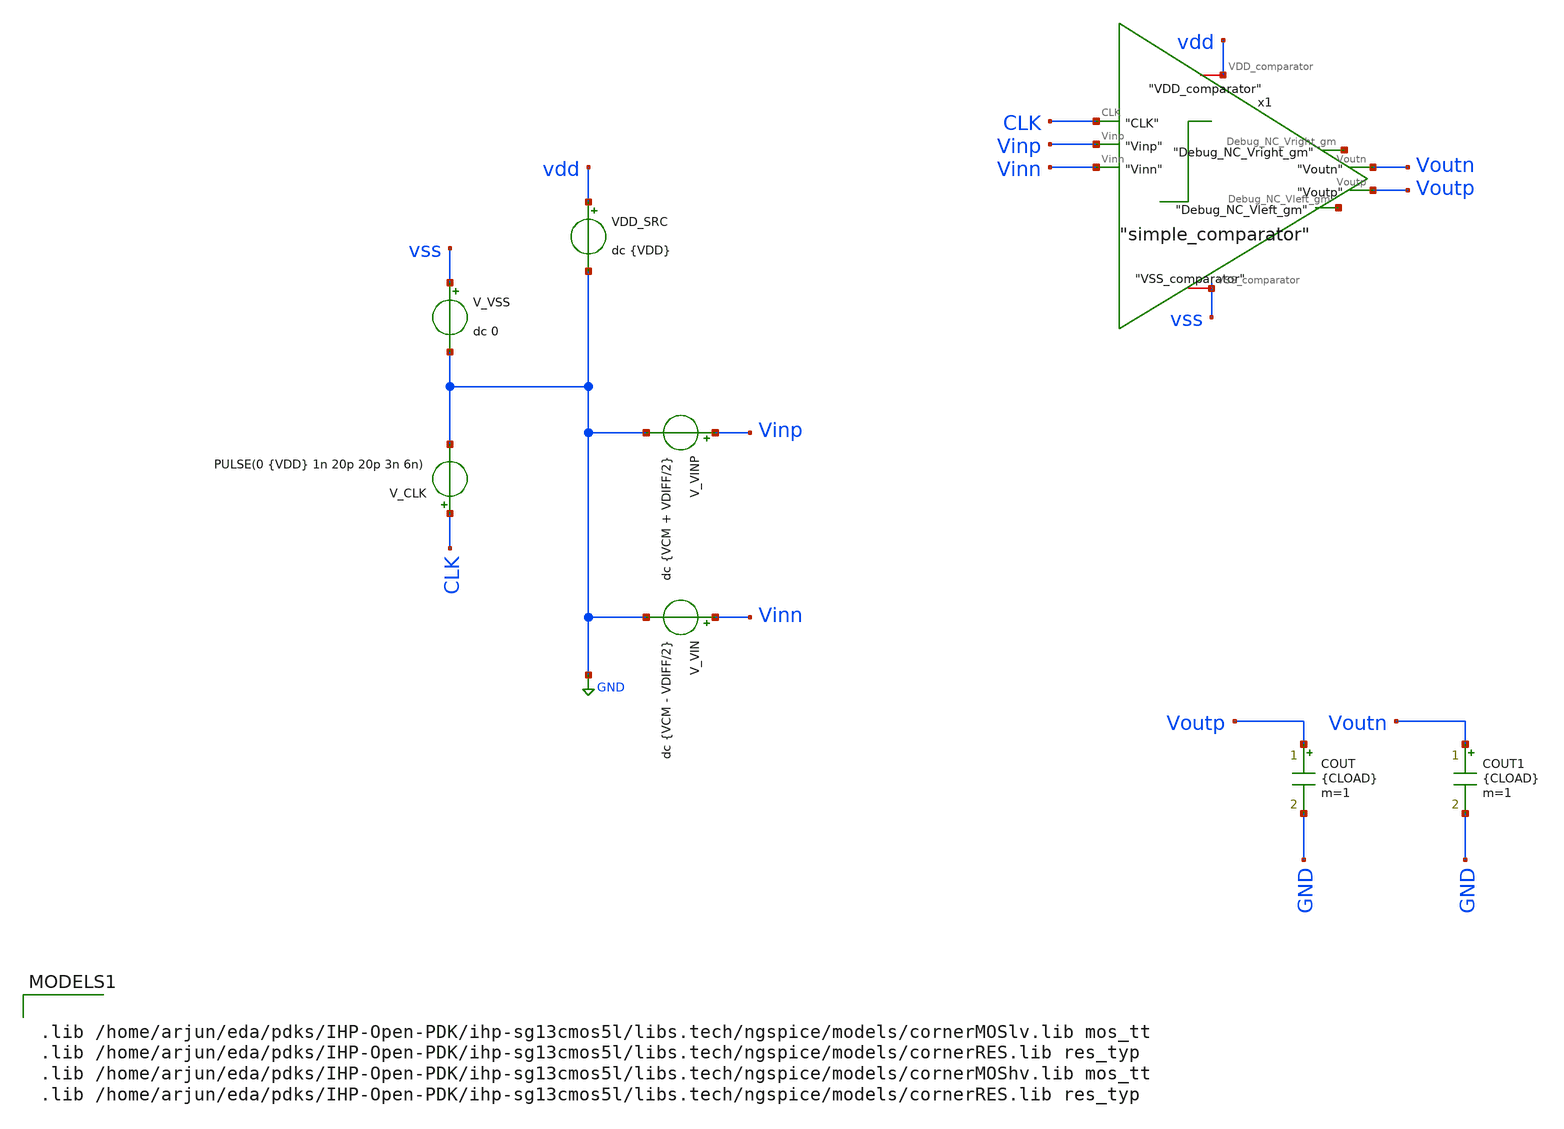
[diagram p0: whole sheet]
** sch_path: circuit_files/xschem_symbols/comp_tb.sch
**.subckt comp_tb
V_VIN Vinn GND dc {VCM - VDIFF/2}
VDD_SRC vdd GND dc {VDD}
V_VINP Vinp GND dc {VCM + VDIFF/2}
V_VSS vss GND dc 0
V_CLK CLK GND PULSE(0 {VDD} 1n 20p 20p 3n 6n)
COUT Voutp GND {CLOAD} m=1
COUT1 Voutn GND {CLOAD} m=1
x1 vdd CLK Voutn Voutp net1 net2 Vinp Vinn vss simple_comparator
**** begin user architecture code

.lib /home/arjun/eda/pdks/IHP-Open-PDK/ihp-sg13cmos5l/libs.tech/ngspice/models/cornerMOSlv.lib mos_tt
.lib /home/arjun/eda/pdks/IHP-Open-PDK/ihp-sg13cmos5l/libs.tech/ngspice/models/cornerRES.lib res_typ
.lib /home/arjun/eda/pdks/IHP-Open-PDK/ihp-sg13cmos5l/libs.tech/ngspice/models/cornerMOShv.lib mos_tt
.lib /home/arjun/eda/pdks/IHP-Open-PDK/ihp-sg13cmos5l/libs.tech/ngspice/models/cornerRES.lib res_typ



.param VDD=3.3
.param VCM=1.65
.param VREF=3.3
.param NBITS=10
.param VLSB=3.22265625e-3
.param VHLSB=1.611328125e-3
.param VDIFF=10e-3
.param CLOAD=20f

.options savecurrents
.options reltol=1e-4 abstol=1e-12 vntol=1e-6 method=gear

.save v(CLK) v(Vinp) v(Vinn) v(Voutp) v(Voutn)
.save v(x1.net1) v(x1.net2) v(x1.net3) v(x1.net4) v(x1.vs_dp)
.save i(VDD_SRC)

.control

alterparam VDD=3.3
alterparam VCM=1.65
alterparam VDIFF=10e-3
reset

tran 1p 6n

write strong_arm_comp_tb.raw

.endc



**** end user architecture code
**.ends

* expanding   symbol:  simple_comparator.sym # of pins=9
** sym_path: circuit_files/xschem_symbols/simple_comparator.sym
** sch_path: circuit_files/xschem_symbols/simple_comparator.sch
.subckt simple_comparator VDD_comparator CLK Voutn Voutp Debug_NC_Vright_gm Debug_NC_Vleft_gm Vinp
+ Vinn VSS_comparator
*.ipin CLK
*.ipin Vinp
*.iopin VSS_comparator
*.iopin VDD_comparator
*.ipin Vinn
*.opin Debug_NC_Vright_gm
*.opin Debug_NC_Vleft_gm
*.opin Voutp
*.opin Voutn
XM1 net2 net1 VDD_comparator VDD_comparator sg13_hv_pmos w=0.3u l=0.4u ng=1 m=1 mm_ok=1
XM2 Debug_NC_Vleft_gm Vinp VS_dp VSS_comparator sg13_hv_nmos w=0.3u l=0.45u ng=1 m=1 mm_ok=1
XM3 net2 net1 Debug_NC_Vleft_gm VSS_comparator sg13_hv_nmos w=0.3u l=0.45u ng=1 m=1 mm_ok=1
XM4 Debug_NC_Vright_gm Vinn VS_dp VSS_comparator sg13_hv_nmos w=0.3u l=0.45u ng=1 m=1 mm_ok=1
XM5 net1 net2 Debug_NC_Vright_gm VSS_comparator sg13_hv_nmos w=0.3u l=0.45u ng=1 m=1 mm_ok=1
XM6 net1 net2 VDD_comparator VDD_comparator sg13_hv_pmos w=0.3u l=0.4u ng=1 m=1 mm_ok=1
XM7 VS_dp CLK VSS_comparator VSS_comparator sg13_hv_nmos w=0.3u l=0.45u ng=1 m=1 mm_ok=1
XM8 net1 CLK VDD_comparator VDD_comparator sg13_hv_pmos w=0.3u l=0.4u ng=1 m=1 mm_ok=1
XM9 net2 CLK VDD_comparator VDD_comparator sg13_hv_pmos w=0.3u l=0.4u ng=1 m=1 mm_ok=1
XM10 net3 net1 VDD_comparator VDD_comparator sg13_hv_pmos w=0.3u l=0.4u ng=1 m=1 mm_ok=1
XM11 net3 net1 VSS_comparator VSS_comparator sg13_hv_nmos w=0.3u l=0.45u ng=1 m=1 mm_ok=1
XM12 Voutn net3 VDD_comparator VDD_comparator sg13_hv_pmos w=0.3u l=0.4u ng=1 m=1 mm_ok=1
XM13 Voutn net3 VSS_comparator VSS_comparator sg13_hv_nmos w=0.3u l=0.45u ng=1 m=1 mm_ok=1
XM14 net4 net2 VDD_comparator VDD_comparator sg13_hv_pmos w=0.3u l=0.4u ng=1 m=1 mm_ok=1
XM15 net4 net2 VSS_comparator VSS_comparator sg13_hv_nmos w=0.3u l=0.45u ng=1 m=1 mm_ok=1
XM16 Voutp net4 VDD_comparator VDD_comparator sg13_hv_pmos w=0.3u l=0.4u ng=1 m=1 mm_ok=1
XM17 Voutp net4 VSS_comparator VSS_comparator sg13_hv_nmos w=0.3u l=0.45u ng=1 m=1 mm_ok=1
.ends

.GLOBAL GND
.end
